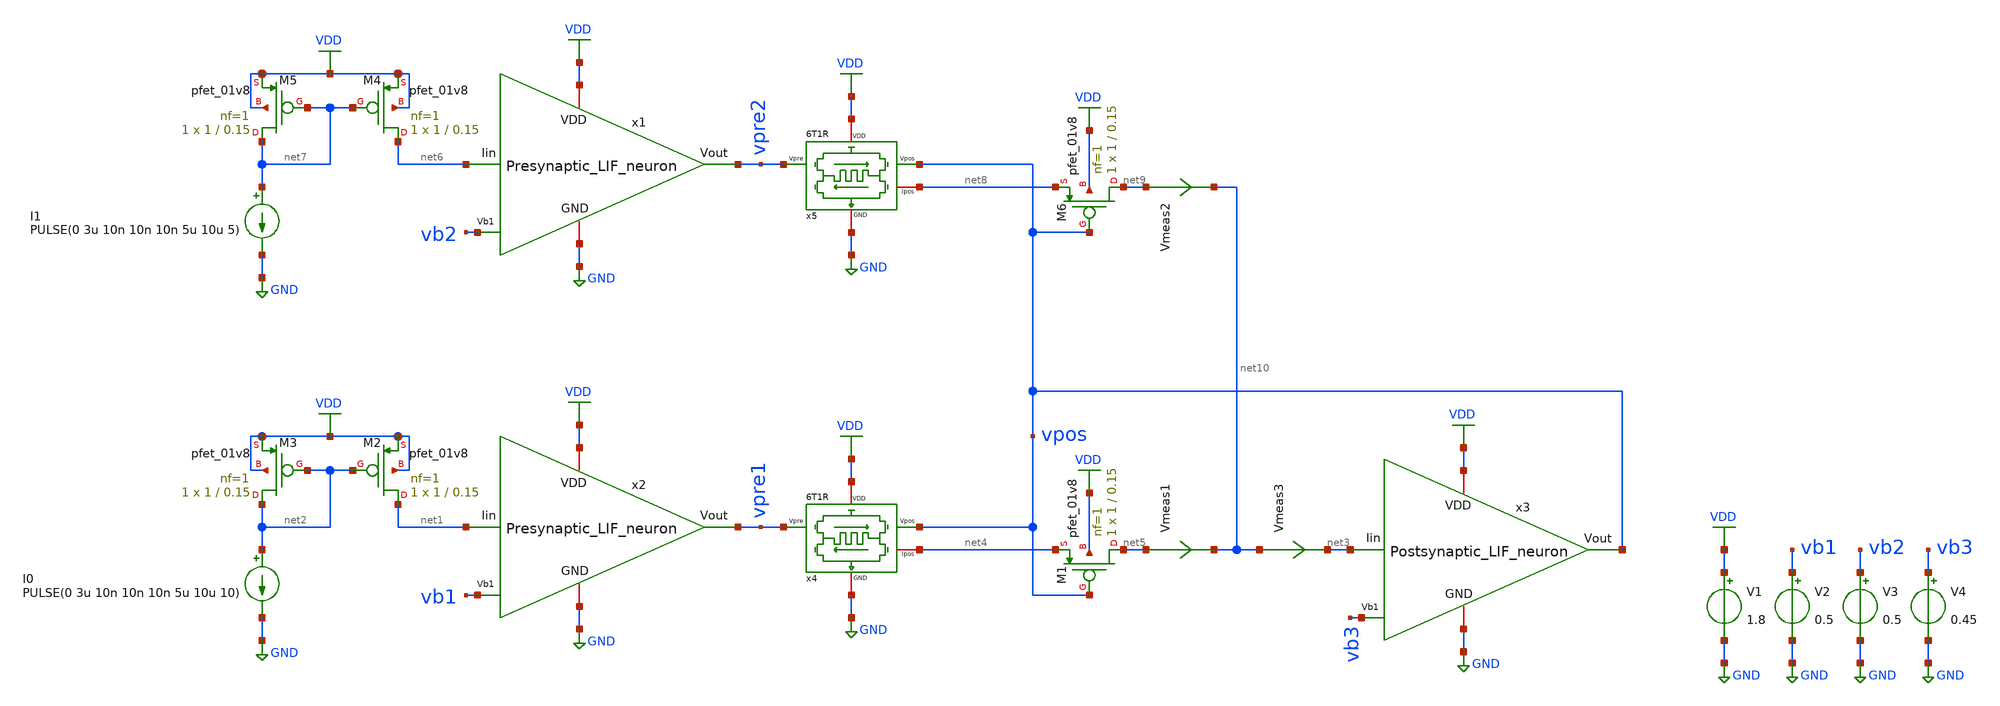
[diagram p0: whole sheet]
** sch_path: STDP/STDP_3_LIF.sch
**.subckt STDP_3_LIF
V1 VDD GND 1.8
V2 vb1 GND 0.5
x4 VDD net4 vpre1 vpos GND 6T1R
I0 net2 GND PULSE(0 3u 10n 10n 10n 5u 10u 10)
XM2 net1 net2 VDD VDD sky130_fd_pr__pfet_01v8 L=0.15 W=1 nf=1 ad='int((nf+1)/2) * W/nf * 0.29' as='int((nf+2)/2) * W/nf * 0.29'
+ pd='2*int((nf+1)/2) * (W/nf + 0.29)' ps='2*int((nf+2)/2) * (W/nf + 0.29)' nrd='0.29 / W' nrs='0.29 / W'
+ sa=0 sb=0 sd=0 mult=1 m=1
XM3 net2 net2 VDD VDD sky130_fd_pr__pfet_01v8 L=0.15 W=1 nf=1 ad='int((nf+1)/2) * W/nf * 0.29' as='int((nf+2)/2) * W/nf * 0.29'
+ pd='2*int((nf+1)/2) * (W/nf + 0.29)' ps='2*int((nf+2)/2) * (W/nf + 0.29)' nrd='0.29 / W' nrs='0.29 / W'
+ sa=0 sb=0 sd=0 mult=1 m=1
XM1 net5 vpos net4 VDD sky130_fd_pr__pfet_01v8 L=0.15 W=1 nf=1 ad='int((nf+1)/2) * W/nf * 0.29' as='int((nf+2)/2) * W/nf * 0.29'
+ pd='2*int((nf+1)/2) * (W/nf + 0.29)' ps='2*int((nf+2)/2) * (W/nf + 0.29)' nrd='0.29 / W' nrs='0.29 / W'
+ sa=0 sb=0 sd=0 mult=1 m=1
Vmeas1 net5 net10 0
.save i(vmeas1)
V3 vb2 GND 0.5
x5 VDD net8 vpre2 vpos GND 6T1R
I1 net7 GND PULSE(0 3u 10n 10n 10n 5u 10u 5)
XM4 net6 net7 VDD VDD sky130_fd_pr__pfet_01v8 L=0.15 W=1 nf=1 ad='int((nf+1)/2) * W/nf * 0.29' as='int((nf+2)/2) * W/nf * 0.29'
+ pd='2*int((nf+1)/2) * (W/nf + 0.29)' ps='2*int((nf+2)/2) * (W/nf + 0.29)' nrd='0.29 / W' nrs='0.29 / W'
+ sa=0 sb=0 sd=0 mult=1 m=1
XM5 net7 net7 VDD VDD sky130_fd_pr__pfet_01v8 L=0.15 W=1 nf=1 ad='int((nf+1)/2) * W/nf * 0.29' as='int((nf+2)/2) * W/nf * 0.29'
+ pd='2*int((nf+1)/2) * (W/nf + 0.29)' ps='2*int((nf+2)/2) * (W/nf + 0.29)' nrd='0.29 / W' nrs='0.29 / W'
+ sa=0 sb=0 sd=0 mult=1 m=1
XM6 net9 vpos net8 VDD sky130_fd_pr__pfet_01v8 L=0.15 W=1 nf=1 ad='int((nf+1)/2) * W/nf * 0.29' as='int((nf+2)/2) * W/nf * 0.29'
+ pd='2*int((nf+1)/2) * (W/nf + 0.29)' ps='2*int((nf+2)/2) * (W/nf + 0.29)' nrd='0.29 / W' nrs='0.29 / W'
+ sa=0 sb=0 sd=0 mult=1 m=1
Vmeas2 net9 net10 0
.save i(vmeas2)
V4 vb3 GND 0.45
Vmeas3 net10 net3 0
.save i(vmeas3)
x1 VDD vpre2 vb2 GND net6 Presynaptic_LIF_neuron
x2 VDD vpre1 vb1 GND net1 Presynaptic_LIF_neuron
x3 net3 VDD vpos vb3 GND Postsynaptic_LIF_neuron
**** begin user architecture code
.lib $::SKYWATER_MODELS/sky130.lib.spice tt

** opencircuitdesign pdks install
.inc $::SKYWATER_MODELS/rram_v0.spice



.control
  save all
  tran 20n 100u
  write STDP_3_LIF.raw
.endc


**** end user architecture code
**.ends

* expanding   symbol:  /home/ricardo/RATT_repos/Proyectos_xschem/synapse/6T1R.sym # of pins=5
** sym_path: synapse/6T1R.sym
** sch_path: synapse/6T1R.sch
.subckt 6T1R VDD Ipos Vpre Vpos GND
*.ipin Vpre
*.ipin Vpos
*.iopin GND
*.iopin Ipos
*.iopin VDD
XM1 vipre Vpre net1 GND sky130_fd_pr__nfet_01v8 L=0.15 W=10 nf=1 ad='int((nf+1)/2) * W/nf * 0.29' as='int((nf+2)/2) * W/nf * 0.29'
+ pd='2*int((nf+1)/2) * (W/nf + 0.29)' ps='2*int((nf+2)/2) * (W/nf + 0.29)' nrd='0.29 / W' nrs='0.29 / W'
+ sa=0 sb=0 sd=0 mult=1 m=1
XR1 net2 net1 rram_v0
XM3 vipre Vpos net2 GND sky130_fd_pr__nfet_01v8 L=0.15 W=1 nf=1 ad='int((nf+1)/2) * W/nf * 0.29' as='int((nf+2)/2) * W/nf * 0.29'
+ pd='2*int((nf+1)/2) * (W/nf + 0.29)' ps='2*int((nf+2)/2) * (W/nf + 0.29)' nrd='0.29 / W' nrs='0.29 / W'
+ sa=0 sb=0 sd=0 mult=1 m=1
XM6 Ipos vipre VDD VDD sky130_fd_pr__pfet_01v8 L=0.15 W=1 nf=1 ad='int((nf+1)/2) * W/nf * 0.29' as='int((nf+2)/2) * W/nf * 0.29'
+ pd='2*int((nf+1)/2) * (W/nf + 0.29)' ps='2*int((nf+2)/2) * (W/nf + 0.29)' nrd='0.29 / W' nrs='0.29 / W'
+ sa=0 sb=0 sd=0 mult=1 m=1
XM5 vipre vipre VDD VDD sky130_fd_pr__pfet_01v8 L=0.15 W=20 nf=1 ad='int((nf+1)/2) * W/nf * 0.29' as='int((nf+2)/2) * W/nf * 0.29'
+ pd='2*int((nf+1)/2) * (W/nf + 0.29)' ps='2*int((nf+2)/2) * (W/nf + 0.29)' nrd='0.29 / W' nrs='0.29 / W'
+ sa=0 sb=0 sd=0 mult=1 m=1
XM2 net1 Vpos GND GND sky130_fd_pr__nfet_01v8 L=0.15 W=1 nf=1 ad='int((nf+1)/2) * W/nf * 0.29' as='int((nf+2)/2) * W/nf * 0.29'
+ pd='2*int((nf+1)/2) * (W/nf + 0.29)' ps='2*int((nf+2)/2) * (W/nf + 0.29)' nrd='0.29 / W' nrs='0.29 / W'
+ sa=0 sb=0 sd=0 mult=1 m=1
XM4 net2 Vpre GND GND sky130_fd_pr__nfet_01v8 L=0.15 W=10 nf=1 ad='int((nf+1)/2) * W/nf * 0.29' as='int((nf+2)/2) * W/nf * 0.29'
+ pd='2*int((nf+1)/2) * (W/nf + 0.29)' ps='2*int((nf+2)/2) * (W/nf + 0.29)' nrd='0.29 / W' nrs='0.29 / W'
+ sa=0 sb=0 sd=0 mult=1 m=1
.ends


* expanding   symbol:
*+  /home/ricardo/RATT_repos/Proyectos_xschem/LIF_neuron/Presynaptic_LIF_neuron.sym # of pins=5
** sym_path: LIF_neuron/Presynaptic_LIF_neuron.sym
** sch_path: LIF_neuron/Presynaptic_LIF_neuron.sch
.subckt Presynaptic_LIF_neuron VDD Vout Vb1 GND Iin
*.iopin GND
*.ipin Vb1
*.iopin VDD
*.opin Vout
*.ipin Iin
XM13 net2 Vb1 GND GND sky130_fd_pr__nfet_01v8 L=0.5 W=5 nf=1 ad='int((nf+1)/2) * W/nf * 0.29' as='int((nf+2)/2) * W/nf * 0.29'
+ pd='2*int((nf+1)/2) * (W/nf + 0.29)' ps='2*int((nf+2)/2) * (W/nf + 0.29)' nrd='0.29 / W' nrs='0.29 / W'
+ sa=0 sb=0 sd=0 mult=1 m=1
XM12 Crefr net1 net2 GND sky130_fd_pr__nfet_01v8 L=1 W=1 nf=1 ad='int((nf+1)/2) * W/nf * 0.29' as='int((nf+2)/2) * W/nf * 0.29'
+ pd='2*int((nf+1)/2) * (W/nf + 0.29)' ps='2*int((nf+2)/2) * (W/nf + 0.29)' nrd='0.29 / W' nrs='0.29 / W'
+ sa=0 sb=0 sd=0 mult=1 m=1
XM11 Crefr net1 VDD VDD sky130_fd_pr__pfet_01v8 L=1 W=1 nf=1 ad='int((nf+1)/2) * W/nf * 0.29' as='int((nf+2)/2) * W/nf * 0.29'
+ pd='2*int((nf+1)/2) * (W/nf + 0.29)' ps='2*int((nf+2)/2) * (W/nf + 0.29)' nrd='0.29 / W' nrs='0.29 / W'
+ sa=0 sb=0 sd=0 mult=1 m=1
XCrefr Crefr GND sky130_fd_pr__cap_mim_m3_1 W=10 L=1 MF=1 m=1
XM14 Iin Crefr GND GND sky130_fd_pr__nfet_01v8 L=15 W=1 nf=1 ad='int((nf+1)/2) * W/nf * 0.29' as='int((nf+2)/2) * W/nf * 0.29'
+ pd='2*int((nf+1)/2) * (W/nf + 0.29)' ps='2*int((nf+2)/2) * (W/nf + 0.29)' nrd='0.29 / W' nrs='0.29 / W'
+ sa=0 sb=0 sd=0 mult=1 m=1
XCm Iin GND sky130_fd_pr__cap_mim_m3_1 W=10 L=1 MF=50 m=50
XM6 net3 Vout GND GND sky130_fd_pr__nfet_01v8 L=0.5 W=1 nf=1 ad='int((nf+1)/2) * W/nf * 0.29' as='int((nf+2)/2) * W/nf * 0.29'
+ pd='2*int((nf+1)/2) * (W/nf + 0.29)' ps='2*int((nf+2)/2) * (W/nf + 0.29)' nrd='0.29 / W' nrs='0.29 / W'
+ sa=0 sb=0 sd=0 mult=1 m=1
XM7 net1 Iin net3 GND sky130_fd_pr__nfet_01v8 L=1 W=1 nf=1 ad='int((nf+1)/2) * W/nf * 0.29' as='int((nf+2)/2) * W/nf * 0.29'
+ pd='2*int((nf+1)/2) * (W/nf + 0.29)' ps='2*int((nf+2)/2) * (W/nf + 0.29)' nrd='0.29 / W' nrs='0.29 / W'
+ sa=0 sb=0 sd=0 mult=1 m=1
XM8 net1 Iin VDD VDD sky130_fd_pr__pfet_01v8 L=1 W=1 nf=1 ad='int((nf+1)/2) * W/nf * 0.29' as='int((nf+2)/2) * W/nf * 0.29'
+ pd='2*int((nf+1)/2) * (W/nf + 0.29)' ps='2*int((nf+2)/2) * (W/nf + 0.29)' nrd='0.29 / W' nrs='0.29 / W'
+ sa=0 sb=0 sd=0 mult=1 m=1
XM9 Vout net1 net3 GND sky130_fd_pr__nfet_01v8 L=1 W=1 nf=1 ad='int((nf+1)/2) * W/nf * 0.29' as='int((nf+2)/2) * W/nf * 0.29'
+ pd='2*int((nf+1)/2) * (W/nf + 0.29)' ps='2*int((nf+2)/2) * (W/nf + 0.29)' nrd='0.29 / W' nrs='0.29 / W'
+ sa=0 sb=0 sd=0 mult=1 m=1
XM10 Vout net1 VDD VDD sky130_fd_pr__pfet_01v8 L=1 W=5 nf=1 ad='int((nf+1)/2) * W/nf * 0.29' as='int((nf+2)/2) * W/nf * 0.29'
+ pd='2*int((nf+1)/2) * (W/nf + 0.29)' ps='2*int((nf+2)/2) * (W/nf + 0.29)' nrd='0.29 / W' nrs='0.29 / W'
+ sa=0 sb=0 sd=0 mult=1 m=1
.ends


* expanding   symbol:
*+  /home/ricardo/RATT_repos/Proyectos_xschem/LIF_neuron/Postsynaptic_LIF_neuron.sym # of pins=5
** sym_path: LIF_neuron/Postsynaptic_LIF_neuron.sym
** sch_path: LIF_neuron/Postsynaptic_LIF_neuron.sch
.subckt Postsynaptic_LIF_neuron Iin VDD Vout Vb1 GND
*.iopin GND
*.ipin Vb1
*.iopin VDD
*.opin Vout
*.ipin Iin
XM13 net2 Vb1 GND GND sky130_fd_pr__nfet_01v8 L=0.5 W=5 nf=1 ad='int((nf+1)/2) * W/nf * 0.29' as='int((nf+2)/2) * W/nf * 0.29'
+ pd='2*int((nf+1)/2) * (W/nf + 0.29)' ps='2*int((nf+2)/2) * (W/nf + 0.29)' nrd='0.29 / W' nrs='0.29 / W'
+ sa=0 sb=0 sd=0 mult=1 m=1
XM12 Crefr net1 net2 GND sky130_fd_pr__nfet_01v8 L=1 W=1 nf=1 ad='int((nf+1)/2) * W/nf * 0.29' as='int((nf+2)/2) * W/nf * 0.29'
+ pd='2*int((nf+1)/2) * (W/nf + 0.29)' ps='2*int((nf+2)/2) * (W/nf + 0.29)' nrd='0.29 / W' nrs='0.29 / W'
+ sa=0 sb=0 sd=0 mult=1 m=1
XM11 Crefr net1 VDD VDD sky130_fd_pr__pfet_01v8 L=1 W=1 nf=1 ad='int((nf+1)/2) * W/nf * 0.29' as='int((nf+2)/2) * W/nf * 0.29'
+ pd='2*int((nf+1)/2) * (W/nf + 0.29)' ps='2*int((nf+2)/2) * (W/nf + 0.29)' nrd='0.29 / W' nrs='0.29 / W'
+ sa=0 sb=0 sd=0 mult=1 m=1
XC1 Crefr GND sky130_fd_pr__cap_mim_m3_1 W=21 L=1 MF=1 m=1
XM14 Iin Crefr GND GND sky130_fd_pr__nfet_01v8 L=20 W=1 nf=1 ad='int((nf+1)/2) * W/nf * 0.29' as='int((nf+2)/2) * W/nf * 0.29'
+ pd='2*int((nf+1)/2) * (W/nf + 0.29)' ps='2*int((nf+2)/2) * (W/nf + 0.29)' nrd='0.29 / W' nrs='0.29 / W'
+ sa=0 sb=0 sd=0 mult=1 m=1
XC2 Iin GND sky130_fd_pr__cap_mim_m3_1 W=30 L=1 MF=50 m=50
XM6 net3 Vout GND GND sky130_fd_pr__nfet_01v8 L=0.5 W=1 nf=1 ad='int((nf+1)/2) * W/nf * 0.29' as='int((nf+2)/2) * W/nf * 0.29'
+ pd='2*int((nf+1)/2) * (W/nf + 0.29)' ps='2*int((nf+2)/2) * (W/nf + 0.29)' nrd='0.29 / W' nrs='0.29 / W'
+ sa=0 sb=0 sd=0 mult=1 m=1
XM7 net1 Iin net3 GND sky130_fd_pr__nfet_01v8 L=1 W=1 nf=1 ad='int((nf+1)/2) * W/nf * 0.29' as='int((nf+2)/2) * W/nf * 0.29'
+ pd='2*int((nf+1)/2) * (W/nf + 0.29)' ps='2*int((nf+2)/2) * (W/nf + 0.29)' nrd='0.29 / W' nrs='0.29 / W'
+ sa=0 sb=0 sd=0 mult=1 m=1
XM8 net1 Iin VDD VDD sky130_fd_pr__pfet_01v8 L=1 W=1 nf=1 ad='int((nf+1)/2) * W/nf * 0.29' as='int((nf+2)/2) * W/nf * 0.29'
+ pd='2*int((nf+1)/2) * (W/nf + 0.29)' ps='2*int((nf+2)/2) * (W/nf + 0.29)' nrd='0.29 / W' nrs='0.29 / W'
+ sa=0 sb=0 sd=0 mult=1 m=1
XM9 Vout net1 net3 GND sky130_fd_pr__nfet_01v8 L=1 W=1 nf=1 ad='int((nf+1)/2) * W/nf * 0.29' as='int((nf+2)/2) * W/nf * 0.29'
+ pd='2*int((nf+1)/2) * (W/nf + 0.29)' ps='2*int((nf+2)/2) * (W/nf + 0.29)' nrd='0.29 / W' nrs='0.29 / W'
+ sa=0 sb=0 sd=0 mult=1 m=1
XM10 Vout net1 VDD VDD sky130_fd_pr__pfet_01v8 L=1 W=5 nf=1 ad='int((nf+1)/2) * W/nf * 0.29' as='int((nf+2)/2) * W/nf * 0.29'
+ pd='2*int((nf+1)/2) * (W/nf + 0.29)' ps='2*int((nf+2)/2) * (W/nf + 0.29)' nrd='0.29 / W' nrs='0.29 / W'
+ sa=0 sb=0 sd=0 mult=1 m=1
.ends

.GLOBAL GND
.GLOBAL VDD
.end
